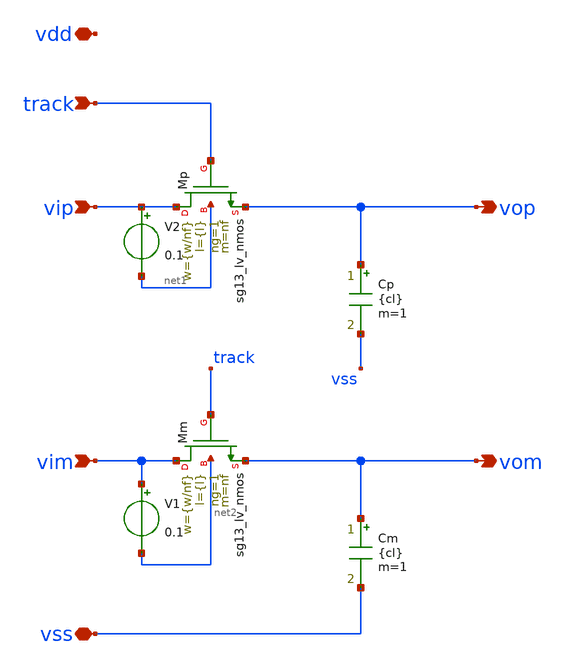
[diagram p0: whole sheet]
** sch_path: th_nmos/xschem/th_nmos_bulk.sch
**.subckt th_nmos_bulk vip vop vim vom track vss vdd
*.ipin vip
*.opin vop
*.ipin vim
*.opin vom
*.ipin track
*.iopin vss
*.iopin vdd
XMp vip track vop net1 sg13_lv_nmos w={w/nf} l={l} ng=1 m=nf mm_ok=1
Cp vop vss {cl} m=1
XMm vim track vom net2 sg13_lv_nmos w={w/nf} l={l} ng=1 m=nf mm_ok=1
Cm vom vss {cl} m=1
V1 vim net2 0.1
V2 vip net1 0.1
**.ends
.end
